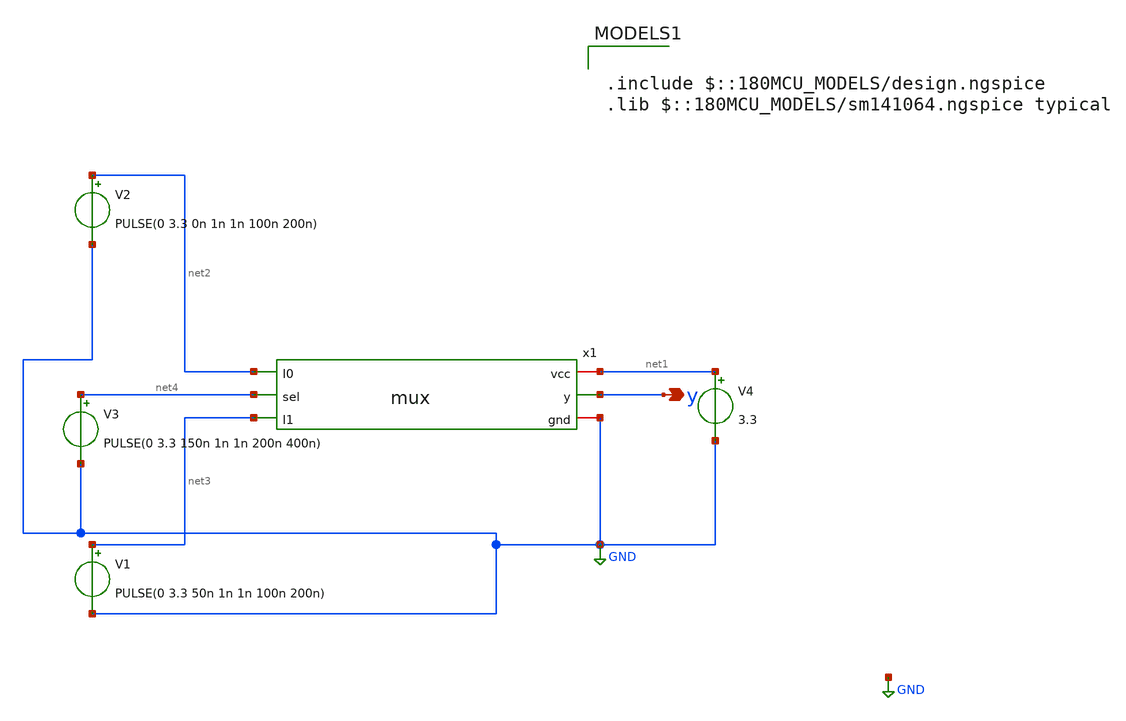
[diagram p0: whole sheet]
** sch_path: designs/schematics/mux2x1/mux_tb.sch
**.subckt mux_tb y
*.opin y
V4 net1 GND 3.3
V3 net4 GND PULSE(0 3.3 150n 1n 1n 200n 400n)
V1 net3 GND PULSE(0 3.3 50n 1n 1n 100n 200n)
V2 net2 GND PULSE(0 3.3 0n 1n 1n 100n 200n)
x1 net1 net2 net4 y net3 GND mux
**** begin user architecture code


.options method=trap rawfile=binary
.options solver=klu nomod
.control
save all

tran 1n 500n

write mux_tb.raw
.endc



.include $::180MCU_MODELS/design.ngspice
.lib $::180MCU_MODELS/sm141064.ngspice typical

**** end user architecture code
**.ends

* expanding   symbol:  voidwalkers-scandff-gf180mcu/designs/schematics/mux2x1/mux.sym # of pins=6
** sym_path: designs/schematics/mux2x1/mux.sym
** sch_path: designs/schematics/mux2x1/mux.sch
.subckt mux vcc I0 sel y I1 gnd
*.ipin I0
*.ipin I1
*.opin y
*.iopin vcc
*.iopin gnd
*.ipin sel
x3 vcc sel net1 gnd inv
x4 vcc I0 sel y gnd net1 tg
x1 vcc I1 net1 y gnd sel tg
.ends


* expanding   symbol:  voidwalkers-scandff-gf180mcu/designs/schematics/mux2x1/inv.sym # of pins=4
** sym_path: designs/schematics/mux2x1/inv.sym
** sch_path: designs/schematics/mux2x1/inv.sch
.subckt inv vcc in out gnd
*.ipin in
*.opin out
*.iopin vcc
*.iopin gnd
XM2 out in vcc vcc pfet_03v3 L=0.28u W=0.22u nf=1 ad='int((nf+1)/2) * W/nf * 0.18u' as='int((nf+2)/2) * W/nf * 0.18u'
+ pd='2*int((nf+1)/2) * (W/nf + 0.18u)' ps='2*int((nf+2)/2) * (W/nf + 0.18u)' nrd='0.18u / W' nrs='0.18u / W'
+ sa=0 sb=0 sd=0 m=1
XM1 out in gnd gnd nfet_03v3 L=0.28u W=0.22u nf=1 ad='int((nf+1)/2) * W/nf * 0.18u' as='int((nf+2)/2) * W/nf * 0.18u'
+ pd='2*int((nf+1)/2) * (W/nf + 0.18u)' ps='2*int((nf+2)/2) * (W/nf + 0.18u)' nrd='0.18u / W' nrs='0.18u / W'
+ sa=0 sb=0 sd=0 m=1
.ends


* expanding   symbol:  voidwalkers-scandff-gf180mcu/designs/schematics/mux2x1/tg.sym # of pins=6
** sym_path: designs/schematics/mux2x1/tg.sym
** sch_path: designs/schematics/mux2x1/tg.sch
.subckt tg vcc A ENB Y gnd EN
*.ipin A
*.ipin EN
*.opin Y
*.ipin ENB
*.iopin gnd
*.iopin vcc
XM1 Y EN A gnd nfet_03v3 L=0.28u W=0.22u nf=1 ad='int((nf+1)/2) * W/nf * 0.18u' as='int((nf+2)/2) * W/nf * 0.18u'
+ pd='2*int((nf+1)/2) * (W/nf + 0.18u)' ps='2*int((nf+2)/2) * (W/nf + 0.18u)' nrd='0.18u / W' nrs='0.18u / W'
+ sa=0 sb=0 sd=0 m=1
XM3 Y ENB A vcc pfet_03v3 L=0.28u W=0.22u nf=1 ad='int((nf+1)/2) * W/nf * 0.18u' as='int((nf+2)/2) * W/nf * 0.18u'
+ pd='2*int((nf+1)/2) * (W/nf + 0.18u)' ps='2*int((nf+2)/2) * (W/nf + 0.18u)' nrd='0.18u / W' nrs='0.18u / W'
+ sa=0 sb=0 sd=0 m=1
.ends

.GLOBAL GND
.end
